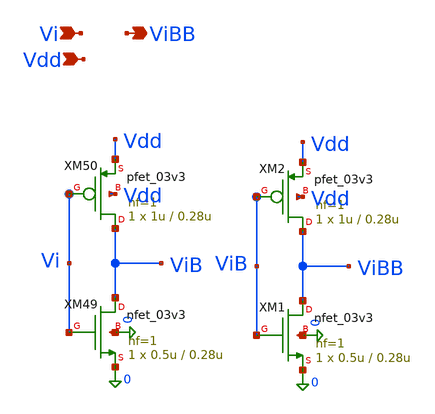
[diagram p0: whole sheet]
** sch_path: blocks/dac/common/cmos_buf.sch
**.subckt cmos_buf Vi ViBB Vdd
*.ipin Vi
*.opin ViBB
*.ipin Vdd
XM49 ViB Vi 0 0 nfet_03v3 L=0.28u W=0.5u nf=1 ad='int((nf+1)/2) * W/nf * 0.18u' as='int((nf+2)/2) * W/nf * 0.18u'
+ pd='2*int((nf+1)/2) * (W/nf + 0.18u)' ps='2*int((nf+2)/2) * (W/nf + 0.18u)' nrd='0.18u / W' nrs='0.18u / W'
+ sa=0 sb=0 sd=0 m=1
XM50 ViB Vi Vdd Vdd pfet_03v3 L=0.28u W=1u nf=1 ad='int((nf+1)/2) * W/nf * 0.18u' as='int((nf+2)/2) * W/nf * 0.18u'
+ pd='2*int((nf+1)/2) * (W/nf + 0.18u)' ps='2*int((nf+2)/2) * (W/nf + 0.18u)' nrd='0.18u / W' nrs='0.18u / W'
+ sa=0 sb=0 sd=0 m=1
XM1 ViBB ViB 0 0 nfet_03v3 L=0.28u W=0.5u nf=1 ad='int((nf+1)/2) * W/nf * 0.18u' as='int((nf+2)/2) * W/nf * 0.18u'
+ pd='2*int((nf+1)/2) * (W/nf + 0.18u)' ps='2*int((nf+2)/2) * (W/nf + 0.18u)' nrd='0.18u / W' nrs='0.18u / W'
+ sa=0 sb=0 sd=0 m=1
XM2 ViBB ViB Vdd Vdd pfet_03v3 L=0.28u W=1u nf=1 ad='int((nf+1)/2) * W/nf * 0.18u' as='int((nf+2)/2) * W/nf * 0.18u'
+ pd='2*int((nf+1)/2) * (W/nf + 0.18u)' ps='2*int((nf+2)/2) * (W/nf + 0.18u)' nrd='0.18u / W' nrs='0.18u / W'
+ sa=0 sb=0 sd=0 m=1
**.ends
.end
